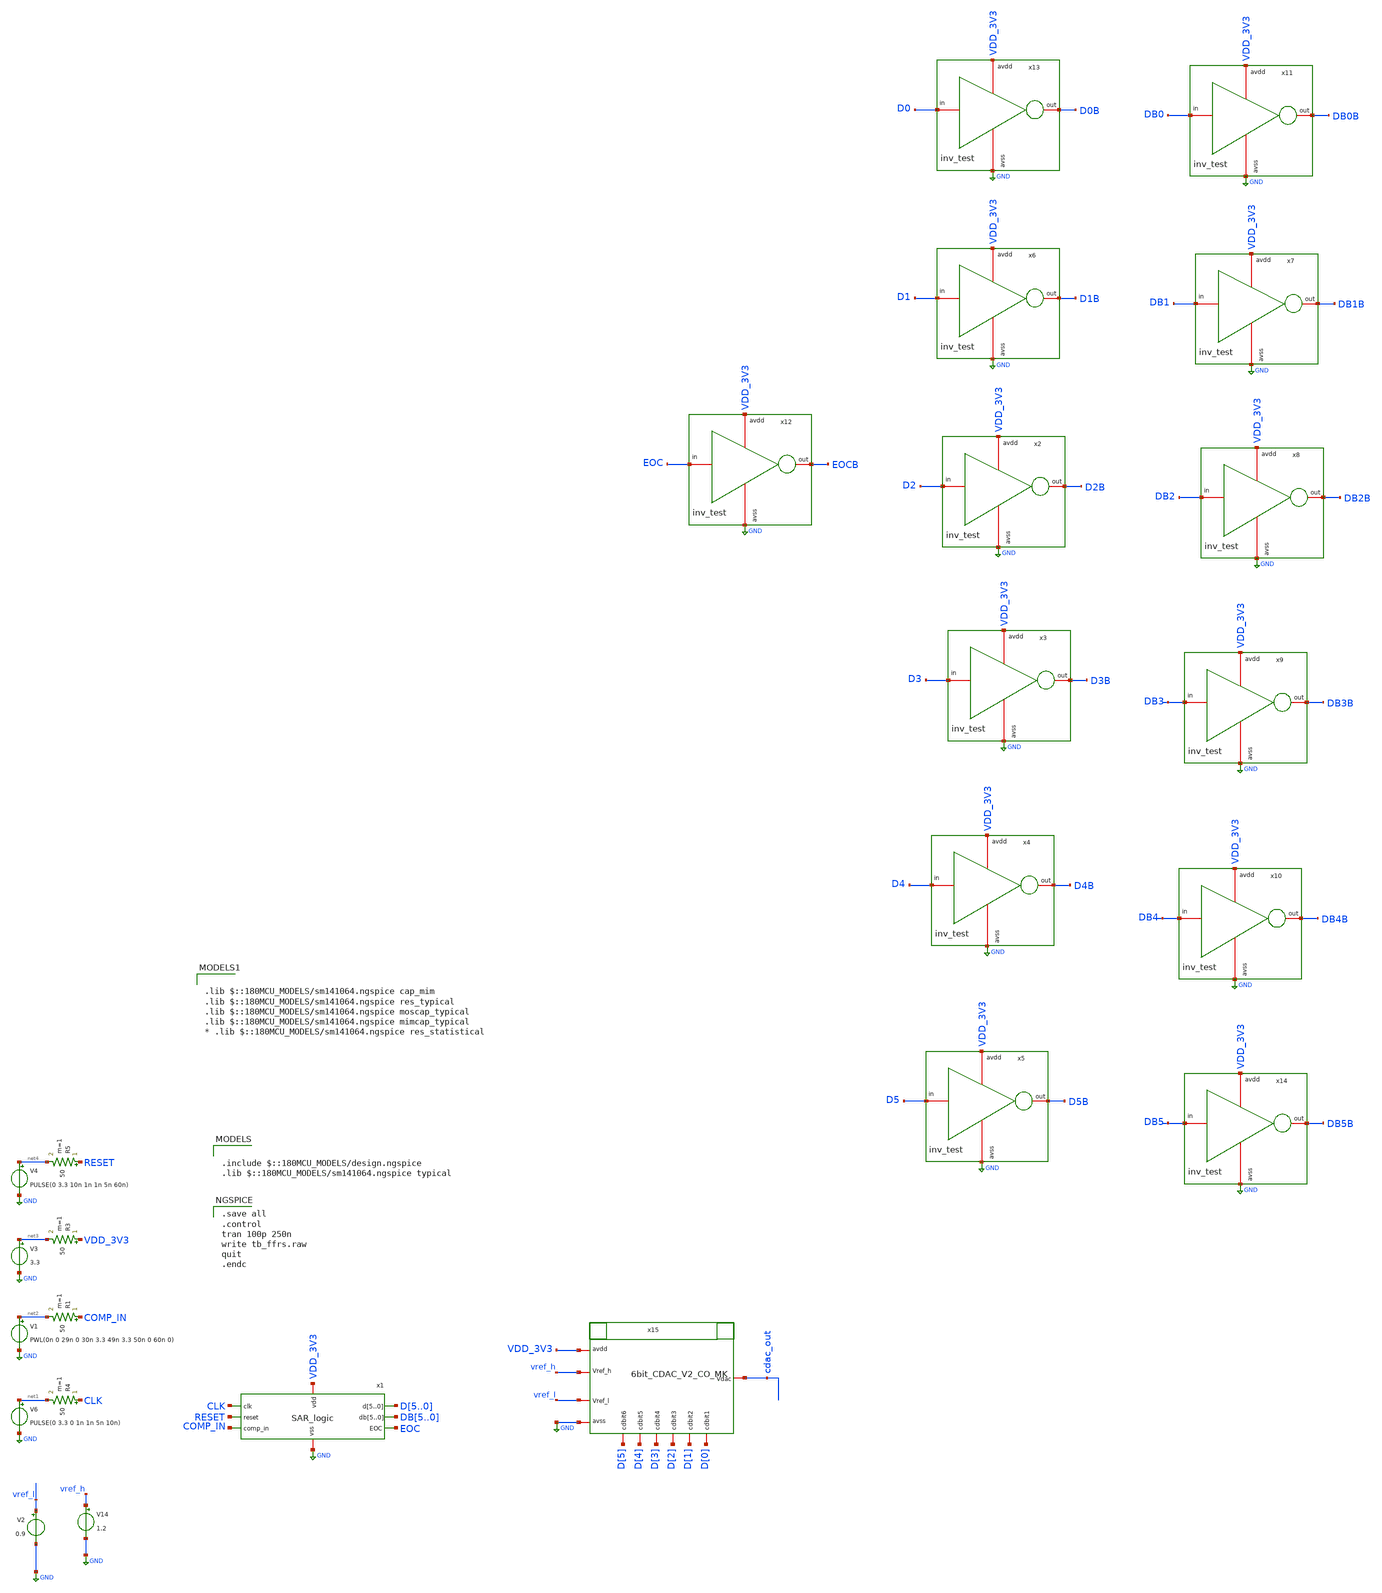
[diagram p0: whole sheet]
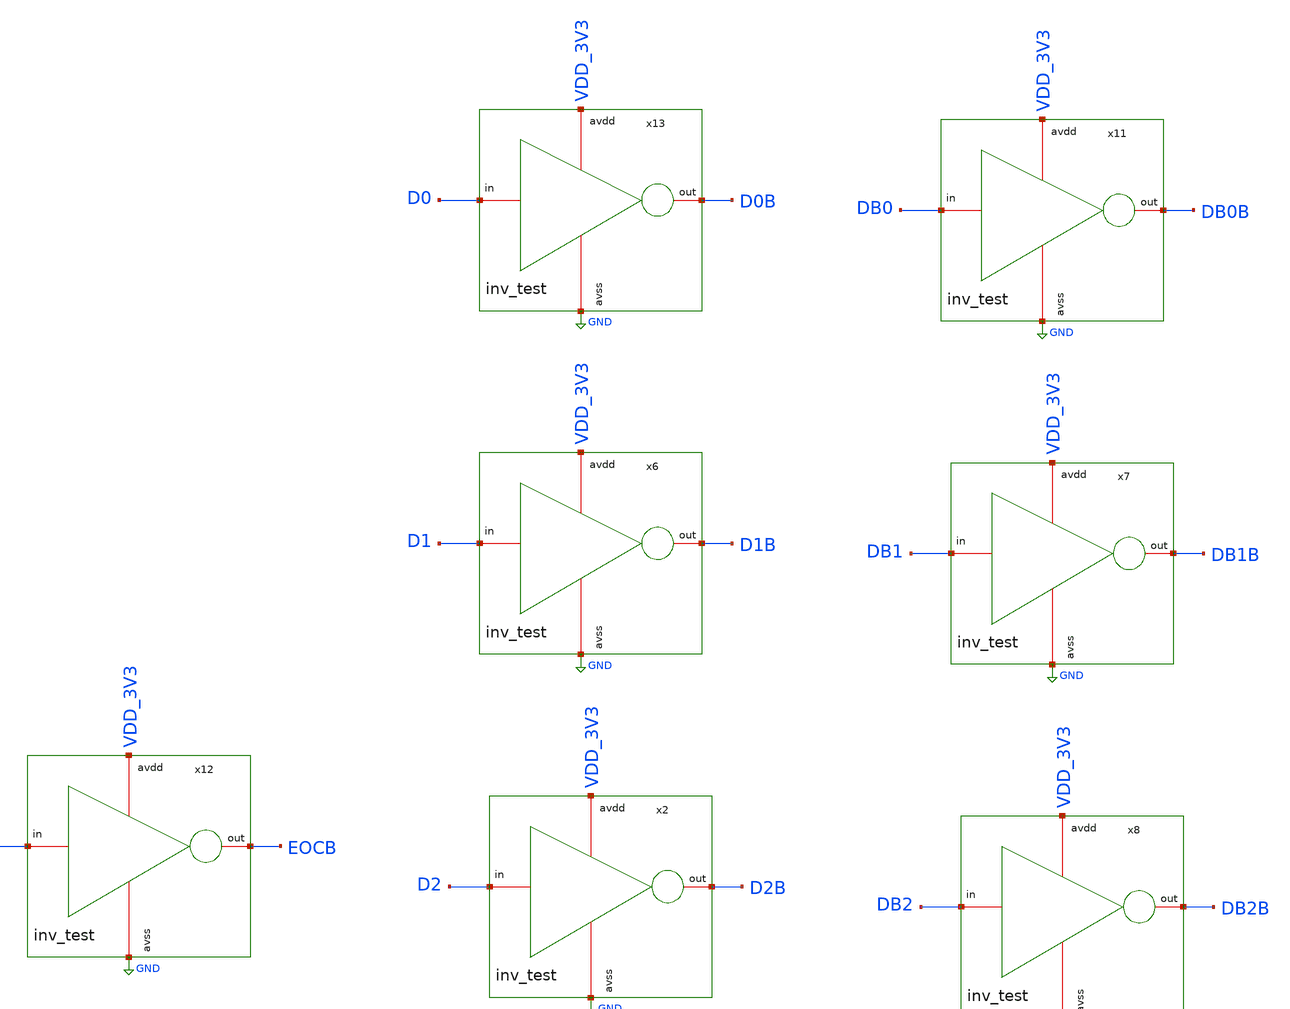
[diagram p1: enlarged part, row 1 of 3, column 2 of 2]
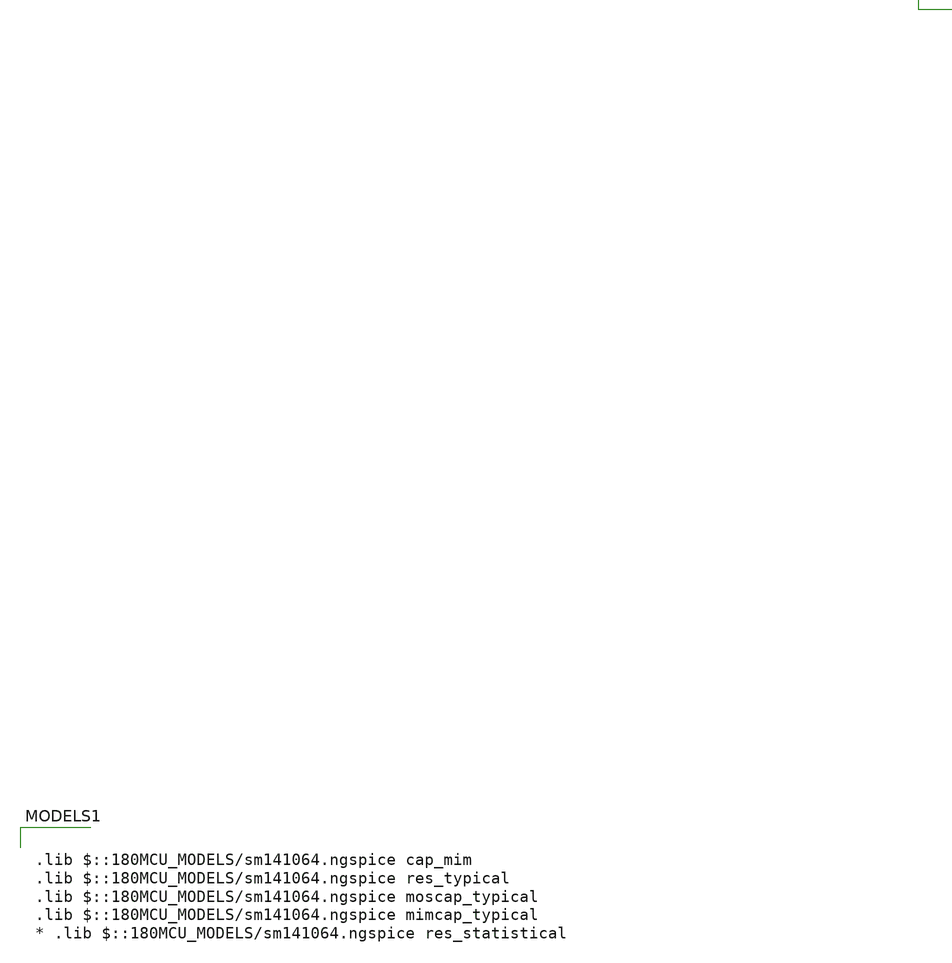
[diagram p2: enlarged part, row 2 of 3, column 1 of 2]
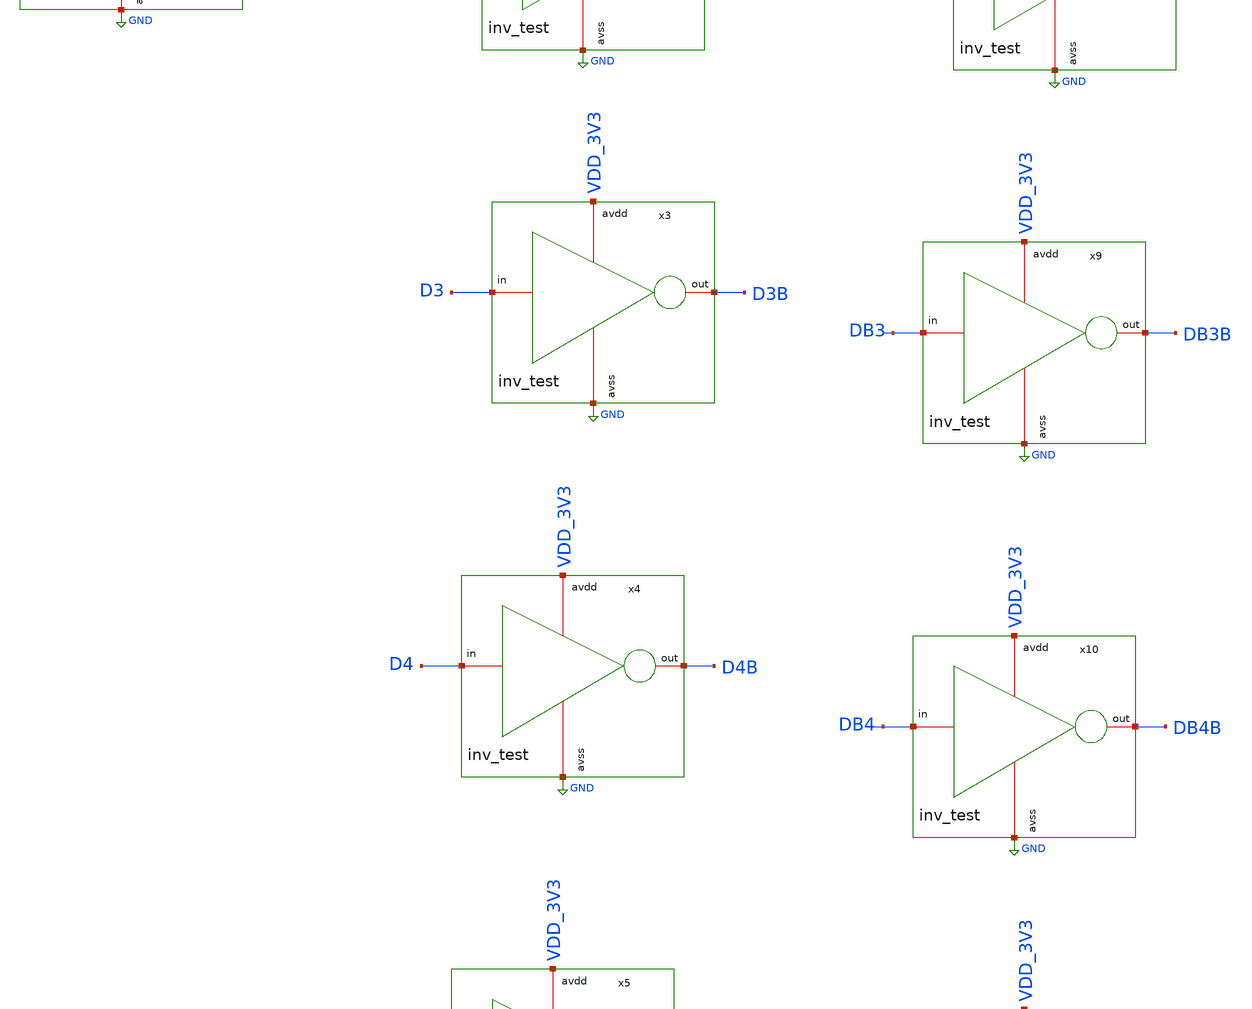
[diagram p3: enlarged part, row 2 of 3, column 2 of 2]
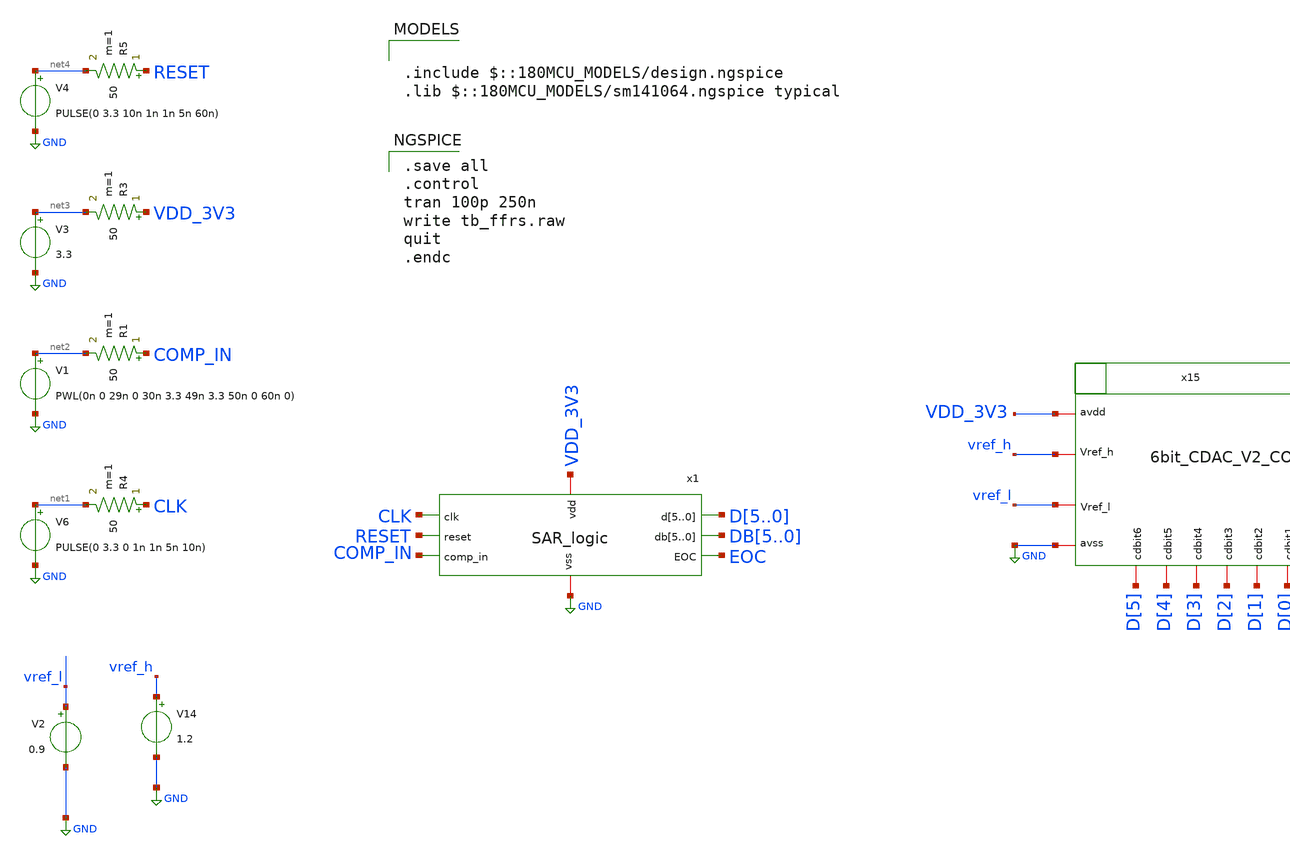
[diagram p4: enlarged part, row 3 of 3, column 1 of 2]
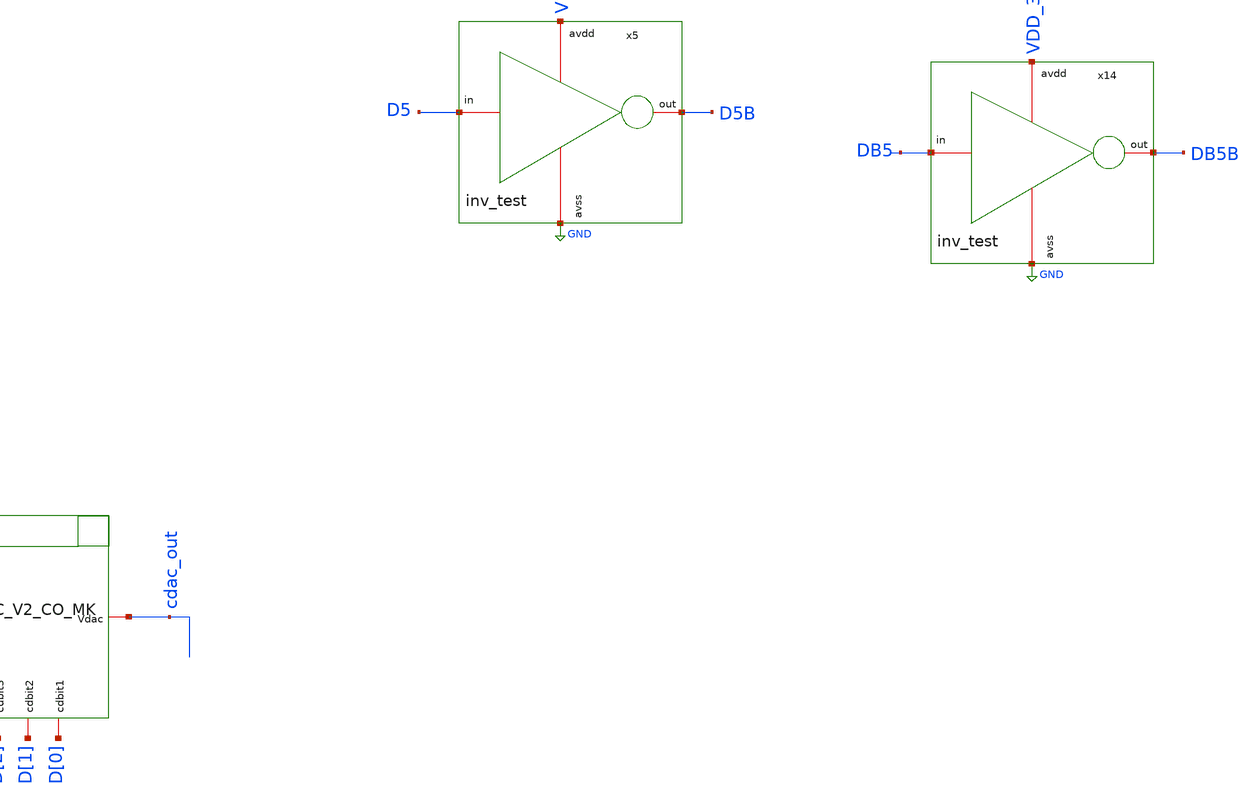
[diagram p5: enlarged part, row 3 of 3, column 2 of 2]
** sch_path: designs/libs/SAR_logic/SAR_logic_inv_output_tb.sch
**.subckt SAR_logic_inv_output_tb
V6 net1 GND PULSE(0 3.3 0 1n 1n 5n 10n)
R4 CLK net1 50 m=1
V1 net2 GND PWL(0n 0 29n 0 30n 3.3 49n 3.3 50n 0 60n 0)
R1 COMP_IN net2 50 m=1
V3 net3 GND 3.3
R3 VDD_3V3 net3 50 m=1
V4 net4 GND PULSE(0 3.3 10n 1n 1n 5n 60n)
R5 RESET net4 50 m=1
x1 VDD_3V3 GND CLK RESET COMP_IN D5 D4 D3 D2 D1 D0 DB5 DB4 DB3 DB2 DB1 DB0 EOC SAR_logic
x2 VDD_3V3 D2 D2B GND inv_test
x3 VDD_3V3 D3 D3B GND inv_test
x4 VDD_3V3 D4 D4B GND inv_test
x5 VDD_3V3 D5 D5B GND inv_test
x6 VDD_3V3 D1 D1B GND inv_test
x7 VDD_3V3 DB1 DB1B GND inv_test
x8 VDD_3V3 DB2 DB2B GND inv_test
x9 VDD_3V3 DB3 DB3B GND inv_test
x10 VDD_3V3 DB4 DB4B GND inv_test
x11 VDD_3V3 DB0 DB0B GND inv_test
x12 VDD_3V3 EOC EOCB GND inv_test
x13 VDD_3V3 D0 D0B GND inv_test
x14 VDD_3V3 DB5 DB5B GND inv_test
V14 vref_h GND 1.2
V2 vref_l GND 0.9
x15 vref_l cdac_out VDD_3V3 GND vref_h D[5] D[4] D[2] D[0] D[1] D[3] 6bit_CDAC_V2_CO_MK
**** begin user architecture code

.include $::180MCU_MODELS/design.ngspice
.lib $::180MCU_MODELS/sm141064.ngspice typical


.save all
.control
tran 100p 250n
write tb_ffrs.raw
quit
.endc


.lib $::180MCU_MODELS/sm141064.ngspice cap_mim
.lib $::180MCU_MODELS/sm141064.ngspice res_typical
.lib $::180MCU_MODELS/sm141064.ngspice moscap_typical
.lib $::180MCU_MODELS/sm141064.ngspice mimcap_typical
* .lib $::180MCU_MODELS/sm141064.ngspice res_statistical

**** end user architecture code
**.ends
.GLOBAL GND
.end
